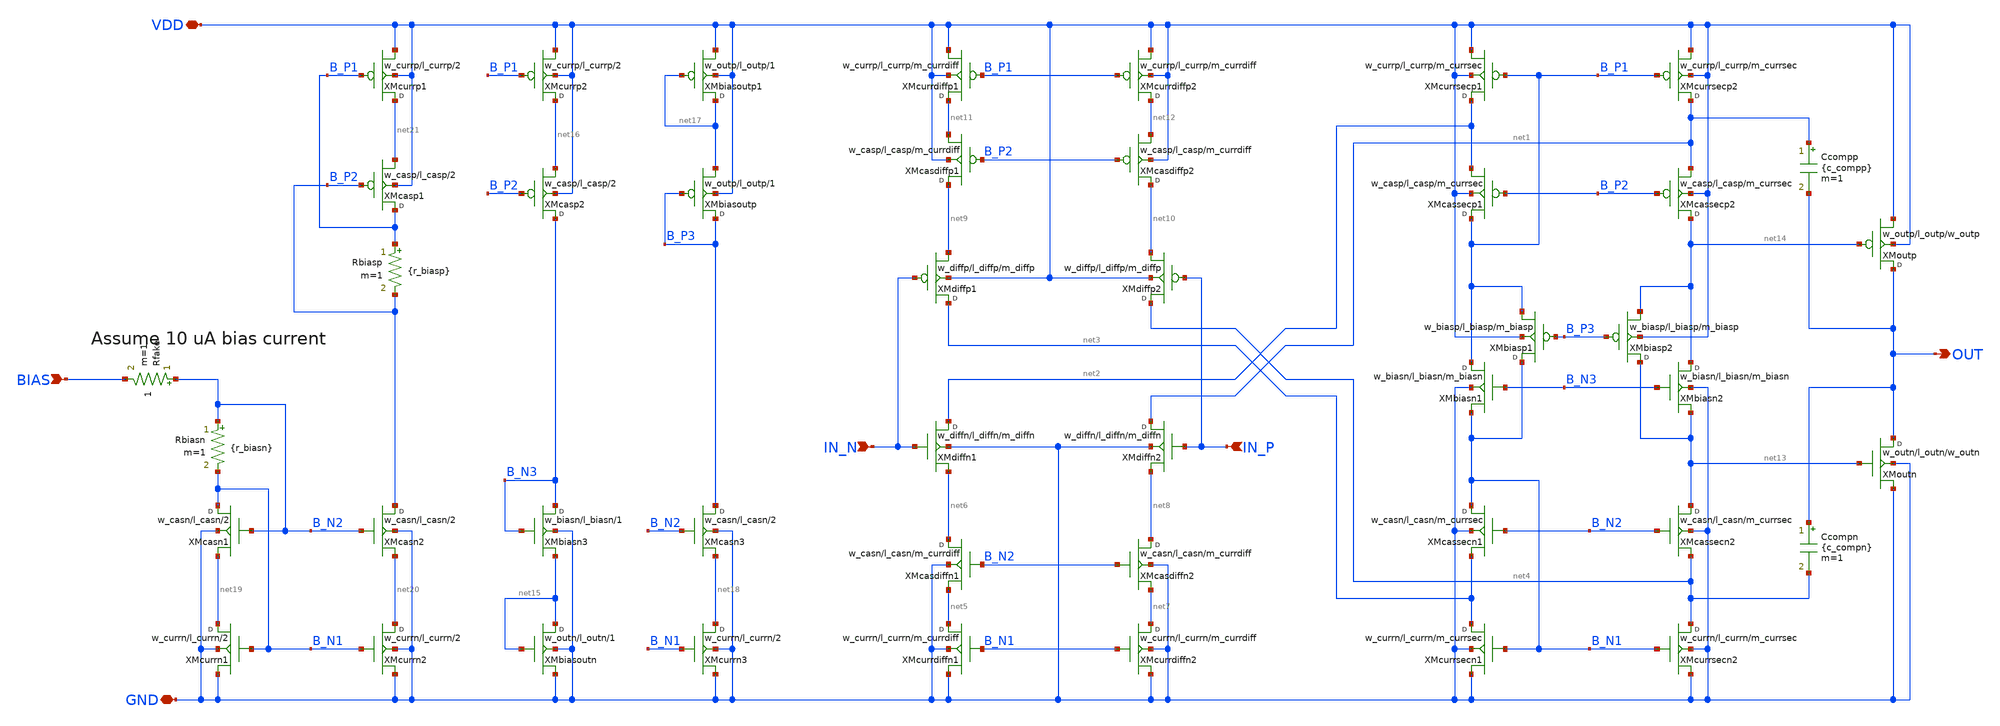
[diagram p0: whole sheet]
** sch_path: design/opamp_rr_100u/opamp_rr_100u.sch
**.subckt opamp_rr_100u BIAS IN_N IN_P OUT VDD GND
*.ipin BIAS
*.ipin IN_N
*.ipin IN_P
*.opin OUT
*.iopin VDD
*.iopin GND
XMdiffn1 net2 IN_N net6 GND ne w=w_diffn l=l_diffn m=m_diffn
XMdiffp1 net3 IN_N net9 VDD pe w=w_diffp l=l_diffp m=m_diffp
XMcasdiffn1 net6 B_N2 net5 GND ne w=w_casn l=l_casn m=m_currdiff
XMcurrdiffn1 net5 B_N1 GND GND ne w=w_currn l=l_currn m=m_currdiff
XMcasdiffn2 net8 B_N2 net7 GND ne w=w_casn l=l_casn m=m_currdiff
XMcurrdiffn2 net7 B_N1 GND GND ne w=w_currn l=l_currn m=m_currdiff
XMdiffn2 net1 IN_P net8 GND ne w=w_diffn l=l_diffn m=m_diffn
XMcurrdiffp2 net12 B_P1 VDD VDD pe w=w_currp l=l_currp m=m_currdiff
XMcurrdiffp1 net11 B_P1 VDD VDD pe w=w_currp l=l_currp m=m_currdiff
XMcasdiffp2 net10 B_P2 net12 VDD pe w=w_casp l=l_casp m=m_currdiff
XMcasdiffp1 net9 B_P2 net11 VDD pe w=w_casp l=l_casp m=m_currdiff
XMdiffp2 net4 IN_P net10 VDD pe w=w_diffp l=l_diffp m=m_diffp
XMbiasp1 B_N1 B_P3 B_P1 VDD pe w=w_biasp l=l_biasp m=m_biasp
XMcurrsecp2 net1 B_P1 VDD VDD pe w=w_currp l=l_currp m=m_currsec
XMcurrsecp1 net2 B_P1 VDD VDD pe w=w_currp l=l_currp m=m_currsec
XMcassecp2 net14 B_P2 net1 VDD pe w=w_casp l=l_casp m=m_currsec
XMcassecp1 B_P1 B_P2 net2 VDD pe w=w_casp l=l_casp m=m_currsec
XMcassecn1 B_N1 B_N2 net3 GND ne w=w_casn l=l_casn m=m_currsec
XMcurrsecn1 net3 B_N1 GND GND ne w=w_currn l=l_currn m=m_currsec
XMcassecn2 net13 B_N2 net4 GND ne w=w_casn l=l_casn m=m_currsec
XMcurrsecn2 net4 B_N1 GND GND ne w=w_currn l=l_currn m=m_currsec
XMbiasp2 net13 B_P3 net14 VDD pe w=w_biasp l=l_biasp m=m_biasp
XMbiasn1 B_P1 B_N3 B_N1 GND ne w=w_biasn l=l_biasn m=m_biasn
XMbiasn2 net14 B_N3 net13 GND ne w=w_biasn l=l_biasn m=m_biasn
XMbiasoutn net15 net15 GND GND ne w=w_outn l=l_outn m=1
XMbiasn3 B_N3 B_N3 net15 GND ne w=w_biasn l=l_biasn m=1
XMcasp2 B_N3 B_P2 net16 VDD pe w=w_casp l=l_casp m=2
XMcurrp2 net16 B_P1 VDD VDD pe w=w_currp l=l_currp m=2
XMcurrn3 net18 B_N1 GND GND ne w=w_currn l=l_currn m=2
XMcasn3 B_P3 B_N2 net18 GND ne w=w_casn l=l_casn m=2
XMbiasoutp B_P3 B_P3 net17 VDD pe w=w_outp l=l_outp m=1
XMbiasoutp1 net17 net17 VDD VDD pe w=w_outp l=l_outp m=1
XMoutn OUT net13 GND GND ne w=w_outn l=l_outn m=w_outn
XMoutp OUT net14 VDD VDD pe w=w_outp l=l_outp m=w_outp
XMcasn1 B_N1 B_N2 net19 GND ne w=w_casn l=l_casn m=2
XMcurrn1 net19 B_N1 GND GND ne w=w_currn l=l_currn m=2
XMcasn2 B_P2 B_N2 net20 GND ne w=w_casn l=l_casn m=2
XMcurrn2 net20 B_N1 GND GND ne w=w_currn l=l_currn m=2
XMcurrp1 net21 B_P1 VDD VDD pe w=w_currp l=l_currp m=2
XMcasp1 B_P1 B_P2 net21 VDD pe w=w_casp l=l_casp m=2
Rbiasn B_N2 B_N1 {r_biasn} m=1
Rbiasp B_P1 B_P2 {r_biasp} m=1
Ccompn OUT net4 {c_compn} m=1
Ccompp net1 OUT {c_compp} m=1
Rfake B_N2 BIAS 1 m=1
**.ends
.end
